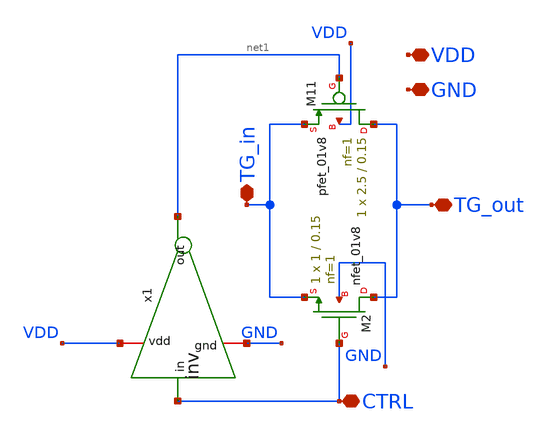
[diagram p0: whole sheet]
** sch_path: sar-adc/updated/TG.sch
**.subckt TG VDD GND CTRL TG_in TG_out
*.iopin VDD
*.iopin GND
*.iopin CTRL
*.iopin TG_in
*.iopin TG_out
XM11 TG_out net1 TG_in VDD sky130_fd_pr__pfet_01v8 L=0.15 W=2.5 nf=1 ad='int((nf+1)/2) * W/nf * 0.29'
+ as='int((nf+2)/2) * W/nf * 0.29' pd='2*int((nf+1)/2) * (W/nf + 0.29)' ps='2*int((nf+2)/2) * (W/nf + 0.29)'
+ nrd='0.29 / W' nrs='0.29 / W' sa=0 sb=0 sd=0 mult=1 m=1
XM2 TG_out CTRL TG_in GND sky130_fd_pr__nfet_01v8 L=0.15 W=1 nf=1 ad='int((1 + 1)/2) * 1 / 1 * 0.29'
+ as='int((1 + 2)/2) * 1 / 1 * 0.29' pd='2*int((1 + 1)/2) * (1 / 1 + 0.29)' ps='2*int((1 + 2)/2) * (1 / 1 + 0.29)'
+ nrd='0.29 / 1 ' nrs='0.29 / 1 ' sa=0 sb=0 sd=0 mult=1 m=1
x1 VDD CTRL net1 GND inv
**.ends

* expanding   symbol:  inv.sym # of pins=4
** sym_path: sar-adc/updated/inv.sym
** sch_path: sar-adc/updated/inv.sch
.subckt inv vdd in out gnd
*.ipin in
*.opin out
*.iopin vdd
*.iopin gnd
XM2 out in gnd gnd sky130_fd_pr__nfet_01v8 L=0.15 W=1 nf=1 ad='int((1 + 1)/2) * 1 / 1 * 0.29' as='int((1 + 2)/2) * 1 / 1 * 0.29'
+ pd='2*int((1 + 1)/2) * (1 / 1 + 0.29)' ps='2*int((1 + 2)/2) * (1 / 1 + 0.29)' nrd='0.29 / 1 ' nrs='0.29 / 1 '
+ sa=0 sb=0 sd=0 mult=1 m=1
XM11 out in vdd vdd sky130_fd_pr__pfet_01v8 L=0.15 W=2.5 nf=1 ad='int((nf+1)/2) * W/nf * 0.29' as='int((nf+2)/2) * W/nf * 0.29'
+ pd='2*int((nf+1)/2) * (W/nf + 0.29)' ps='2*int((nf+2)/2) * (W/nf + 0.29)' nrd='0.29 / W' nrs='0.29 / W'
+ sa=0 sb=0 sd=0 mult=1 m=1
.ends

.end
